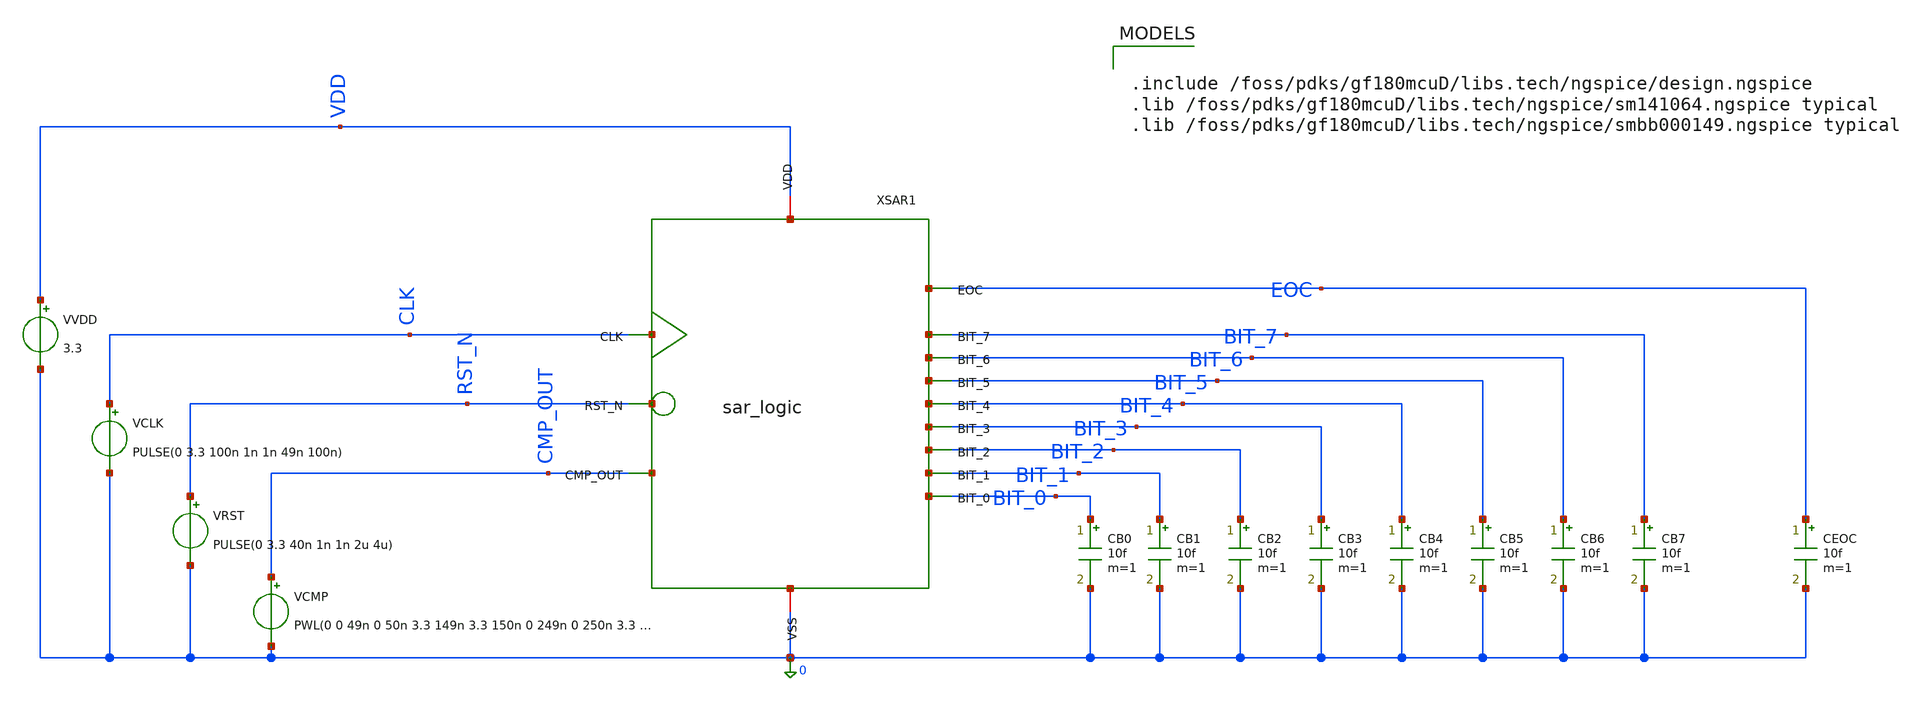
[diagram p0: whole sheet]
** sch_path: sar_logic/sar_designs/tb_sar_logic.sch
**.subckt tb_sar_logic
XSAR1 VDD 0 BIT_7 BIT_6 BIT_5 BIT_4 BIT_3 BIT_2 BIT_1 BIT_0 EOC RST_N CMP_OUT CLK sar_logic
VVDD VDD 0 3.3
VCLK CLK 0 PULSE(0 3.3 100n 1n 1n 49n 100n)
VRST RST_N 0 PULSE(0 3.3 40n 1n 1n 2u 4u)
VCMP CMP_OUT 0 PWL(0 0 49n 0 50n 3.3 149n 3.3 150n 0 249n 0 250n 3.3 349n 3.3 350n 0 449n 0 450n 3.3
+ 549n 3.3 550n 0 649n 0 650n 3.3 749n 3.3 750n 0 1u 0)
CB1 BIT_1 0 10f m=1
CB2 BIT_2 0 10f m=1
CB3 BIT_3 0 10f m=1
CB4 BIT_4 0 10f m=1
CB5 BIT_5 0 10f m=1
CB6 BIT_6 0 10f m=1
CB7 BIT_7 0 10f m=1
CEOC EOC 0 10f m=1
CB0 BIT_0 0 10f m=1
**** begin user architecture code


.include /foss/pdks/gf180mcuD/libs.tech/ngspice/design.ngspice
.lib /foss/pdks/gf180mcuD/libs.tech/ngspice/sm141064.ngspice typical
.lib /foss/pdks/gf180mcuD/libs.tech/ngspice/smbb000149.ngspice typical




.options method=gear reltol=1e-3 abstol=1e-12 vntol=1e-6

.control
  save all
  tran 20p 1u

  * Decode BIT_7 through BIT_0 into an approximately integer-valued waveform.
  * Keep this entire let command on one physical line.
  let sar_code =
+ (128/3.3)*v(BIT_7)+(64/3.3)*v(BIT_6)+(32/3.3)*v(BIT_5)+(16/3.3)*v(BIT_4)+(8/3.3)*v(BIT_3)+(4/3.3)*v(BIT_2)+(2/3.3)*v(BIT_1)+(1/3.3)*v(BIT_0)

  * Sample the walking trial-code sequence.
  meas tran code070 FIND sar_code AT=70n
  meas tran code130 FIND sar_code AT=130n
  meas tran code230 FIND sar_code AT=230n
  meas tran code330 FIND sar_code AT=330n
  meas tran code430 FIND sar_code AT=430n
  meas tran code530 FIND sar_code AT=530n
  meas tran code630 FIND sar_code AT=630n
  meas tran code730 FIND sar_code AT=730n
  meas tran code830 FIND sar_code AT=830n
  meas tran code930 FIND sar_code AT=930n

  * Check EOC before, during, and after completion.
  meas tran eoc070 FIND v(EOC) AT=70n
  meas tran eoc730 FIND v(EOC) AT=730n
  meas tran eoc830 FIND v(EOC) AT=830n
  meas tran eoc930 FIND v(EOC) AT=930n

  * Keep each complete timing measurement on one physical line.
  meas tran tclk8_eoc TRIG v(CLK) VAL=1.65 RISE=8 TARG v(EOC) VAL=1.65 RISE=1
  meas tran eoc_width TRIG v(EOC) VAL=1.65 RISE=1 TARG v(EOC) VAL=1.65 FALL=1

  * Start with a failure value. It is cleared only if the essential
  * measurements were successfully created.
  let failures = 999

  if code930 > -0.5
    if tclk8_eoc > -1
      if eoc_width > 0
        let failures = 0

        * 70 ns: reset-created MSB trial, 10000000 = 128.
        if code070 < 127.5
          echo FAIL_code070_below_128
          let failures = failures + 1
        end
        if code070 > 128.5
          echo FAIL_code070_above_128
          let failures = failures + 1
        end

        * 130 ns: accepted C7 plus bit-6 trial, 11000000 = 192.
        if code130 < 191.5
          echo FAIL_code130_below_192
          let failures = failures + 1
        end
        if code130 > 192.5
          echo FAIL_code130_above_192
          let failures = failures + 1
        end

        * 230 ns: bit-6 rejected and bit-5 trial, 10100000 = 160.
        if code230 < 159.5
          echo FAIL_code230_below_160
          let failures = failures + 1
        end
        if code230 > 160.5
          echo FAIL_code230_above_160
          let failures = failures + 1
        end

        * 330 ns: bit-4 trial, 10110000 = 176.
        if code330 < 175.5
          echo FAIL_code330_below_176
          let failures = failures + 1
        end
        if code330 > 176.5
          echo FAIL_code330_above_176
          let failures = failures + 1
        end

        * 430 ns: bit-4 rejected and bit-3 trial, 10101000 = 168.
        if code430 < 167.5
          echo FAIL_code430_below_168
          let failures = failures + 1
        end
        if code430 > 168.5
          echo FAIL_code430_above_168
          let failures = failures + 1
        end

        * 530 ns: bit-2 trial, 10101100 = 172.
        if code530 < 171.5
          echo FAIL_code530_below_172
          let failures = failures + 1
        end
        if code530 > 172.5
          echo FAIL_code530_above_172
          let failures = failures + 1
        end

        * 630 ns: bit-2 rejected and bit-1 trial, 10101010 = 170.
        if code630 < 169.5
          echo FAIL_code630_below_170
          let failures = failures + 1
        end
        if code630 > 170.5
          echo FAIL_code630_above_170
          let failures = failures + 1
        end

        * 730 ns: bit-0 trial, 10101011 = 171.
        if code730 < 170.5
          echo FAIL_code730_below_171
          let failures = failures + 1
        end
        if code730 > 171.5
          echo FAIL_code730_above_171
          let failures = failures + 1
        end

        * 830 ns: final C0 decision captured, 10101010 = 170.
        if code830 < 169.5
          echo FAIL_code830_below_170
          let failures = failures + 1
        end
        if code830 > 170.5
          echo FAIL_code830_above_170
          let failures = failures + 1
        end

        * 930 ns: EOC clears while the code remains stored.
        if code930 < 169.5
          echo FAIL_code930_below_held_170
          let failures = failures + 1
        end
        if code930 > 170.5
          echo FAIL_code930_above_held_170
          let failures = failures + 1
        end

        * EOC must be low before completion.
        if eoc070 > 0.33
          echo FAIL_EOC_high_at_70ns
          let failures = failures + 1
        end
        if eoc730 > 0.33
          echo FAIL_EOC_high_before_final_capture
          let failures = failures + 1
        end

        * EOC must be high after the eighth clock edge.
        if eoc830 < 2.97
          echo FAIL_EOC_not_high_at_830ns
          let failures = failures + 1
        end

        * EOC must clear after the following edge.
        if eoc930 > 0.33
          echo FAIL_EOC_not_low_at_930ns
          let failures = failures + 1
        end

        * EOC should rise shortly after the eighth clock edge.
        if tclk8_eoc < 0
          echo FAIL_negative_clock_to_EOC_delay
          let failures = failures + 1
        end
        if tclk8_eoc > 10n
          echo FAIL_clock_to_EOC_delay_above_10ns
          let failures = failures + 1
        end

        * EOC should remain high for approximately one 100 ns period.
        if eoc_width < 90n
          echo FAIL_EOC_width_below_90ns
          let failures = failures + 1
        end
        if eoc_width > 110n
          echo FAIL_EOC_width_above_110ns
          let failures = failures + 1
        end
      end
    end
  end

  echo
  echo SAR_SEQUENCE_RESULTS
  print code070 code130 code230 code330 code430
  print code530 code630 code730 code830 code930

  echo
  echo EOC_RESULTS
  print eoc070 eoc730 eoc830 eoc930

  echo
  echo EOC_TIMING
  print tclk8_eoc eoc_width
  echo

  if failures < 0.5
    echo PASS_tb_sar_logic_digital_only
  else
    echo FAIL_tb_sar_logic_digital_only
    print failures
  end

  write tb_sar_logic_digital.raw

  plot v(CLK) v(RST_N) v(CMP_OUT) v(EOC)
  plot v(BIT_7) v(BIT_6) v(BIT_5) v(BIT_4)
  plot v(BIT_3) v(BIT_2) v(BIT_1) v(BIT_0)
.endc


**** end user architecture code
**.ends
.end
